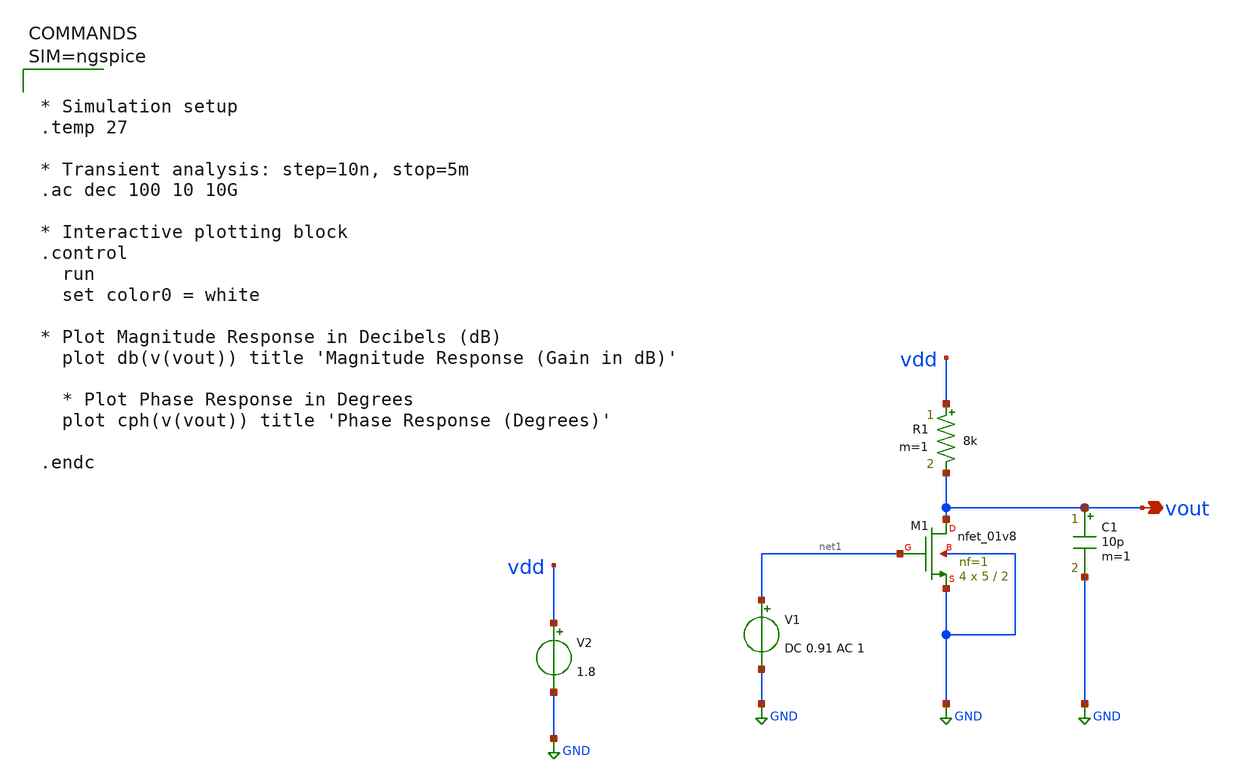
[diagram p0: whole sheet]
** sch_path: testbenches/NMOS_Restitive_Load_gainPlot.sch
**.subckt NMOS_Restitive_Load_gainPlot vout
*.opin vout
XM1 vout net1 GND GND sky130_fd_pr__nfet_01v8 L=2 W=5 nf=1 ad='int((1 + 1)/2) * 5 / 1 * 0.29' as='int((1 + 2)/2) * 5 / 1 * 0.29'
+ pd='2*int((1 + 1)/2) * (5 / 1 + 0.29)' ps='2*int((1 + 2)/2) * (5 / 1 + 0.29)' nrd='0.29 / 5 ' nrs='0.29 / 5 '
+ sa=0 sb=0 sd=0 mult=4 m=4
R1 vdd vout 8k m=1
V1 net1 GND DC 0.91 AC 1
C1 vout GND 10p m=1
V2 vdd GND 1.8
**** begin user architecture code

** opencircuitdesign pdks install
.lib $::SKYWATER_MODELS/sky130.lib.spice tt




* Simulation setup
.temp 27

* Transient analysis: step=10n, stop=5m
.ac dec 100 10 10G

* Interactive plotting block
.control
  run
  set color0 = white

* Plot Magnitude Response in Decibels (dB)
  plot db(v(vout)) title 'Magnitude Response (Gain in dB)'

  * Plot Phase Response in Degrees
  plot cph(v(vout)) title 'Phase Response (Degrees)'

.endc




**** end user architecture code
**.ends
.GLOBAL GND
.end
